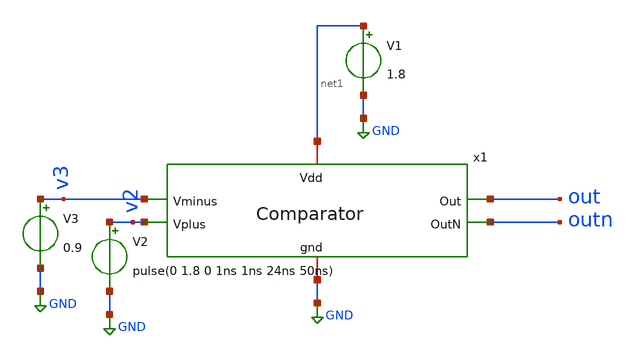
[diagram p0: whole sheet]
** sch_path: xschem/comparator_tb.sch
**.subckt comparator_tb
x1 net1 out outn v3 v2 GND comparator
V1 net1 GND 1.8
V2 v2 GND pulse(0 1.8 0 1ns 1ns 24ns 50ns)
V3 v3 GND 0.9
**** begin user architecture code


.inclue /home/lbraga/Projects/relax_oscillator/mag/comparator.spice
.lib /usr/local/share/pdk/sky130A/libs.tech/ngspice/sky130.lib.spice tt
.control
        tran 0.01n 300ns
  	set color0=rgb:f/f/f
        set xbrushwidth=3
        plot v(v2) v(v3)
	options color3=green
        options color2=orange
	plot v(out) v(outn)
	plot i(v1)
        plot @m.x1.xxm11.x0.msky130_fd_pr__nfet_01v8[id]

.endc
.save all


**** end user architecture code
**.ends

* expanding   symbol:  comparator.sym # of pins=6
** sym_path: xschem/comparator.sym
** sch_path: xschem/comparator.sch
.subckt comparator Vdd Out OutN Vminus Vplus gnd
*.ipin Vminus
*.ipin Vplus
*.iopin Vdd
*.iopin gnd
*.opin OutN
*.opin Out
XM1 net2 net2 Vdd Vdd sky130_fd_pr__pfet_01v8 L=0.75 W=7.5 nf=1 ad='int((nf+1)/2) * W/nf * 0.29' as='int((nf+2)/2) * W/nf * 0.29'
+ pd='2*int((nf+1)/2) * (W/nf + 0.29)' ps='2*int((nf+2)/2) * (W/nf + 0.29)' nrd='0.29 / W' nrs='0.29 / W'
+ sa=0 sb=0 sd=0 mult=1 m=1
XM2 net3 net2 Vdd Vdd sky130_fd_pr__pfet_01v8 L=0.75 W=7.5 nf=1 ad='int((nf+1)/2) * W/nf * 0.29' as='int((nf+2)/2) * W/nf * 0.29'
+ pd='2*int((nf+1)/2) * (W/nf + 0.29)' ps='2*int((nf+2)/2) * (W/nf + 0.29)' nrd='0.29 / W' nrs='0.29 / W'
+ sa=0 sb=0 sd=0 mult=1 m=1
XM5 OutN net3 Vdd Vdd sky130_fd_pr__pfet_01v8 L=0.15 W=1.5 nf=1 ad='int((nf+1)/2) * W/nf * 0.29' as='int((nf+2)/2) * W/nf * 0.29'
+ pd='2*int((nf+1)/2) * (W/nf + 0.29)' ps='2*int((nf+2)/2) * (W/nf + 0.29)' nrd='0.29 / W' nrs='0.29 / W'
+ sa=0 sb=0 sd=0 mult=1 m=1
XM6 OutN net3 gnd gnd sky130_fd_pr__nfet_01v8 L=0.15 W=.75 nf=1 ad='int((nf+1)/2) * W/nf * 0.29' as='int((nf+2)/2) * W/nf * 0.29'
+ pd='2*int((nf+1)/2) * (W/nf + 0.29)' ps='2*int((nf+2)/2) * (W/nf + 0.29)' nrd='0.29 / W' nrs='0.29 / W'
+ sa=0 sb=0 sd=0 mult=1 m=1
XM7 Out OutN Vdd Vdd sky130_fd_pr__pfet_01v8 L=0.15 W=3 nf=1 ad='int((nf+1)/2) * W/nf * 0.29' as='int((nf+2)/2) * W/nf * 0.29'
+ pd='2*int((nf+1)/2) * (W/nf + 0.29)' ps='2*int((nf+2)/2) * (W/nf + 0.29)' nrd='0.29 / W' nrs='0.29 / W'
+ sa=0 sb=0 sd=0 mult=1 m=1
XM8 Out OutN gnd gnd sky130_fd_pr__nfet_01v8 L=0.15 W=1.5 nf=1 ad='int((nf+1)/2) * W/nf * 0.29' as='int((nf+2)/2) * W/nf * 0.29'
+ pd='2*int((nf+1)/2) * (W/nf + 0.29)' ps='2*int((nf+2)/2) * (W/nf + 0.29)' nrd='0.29 / W' nrs='0.29 / W'
+ sa=0 sb=0 sd=0 mult=1 m=1
XM3 net2 Vplus net1 gnd sky130_fd_pr__nfet_01v8 L=0.75 W=3.75 nf=1 ad='int((nf+1)/2) * W/nf * 0.29' as='int((nf+2)/2) * W/nf * 0.29'
+ pd='2*int((nf+1)/2) * (W/nf + 0.29)' ps='2*int((nf+2)/2) * (W/nf + 0.29)' nrd='0.29 / W' nrs='0.29 / W'
+ sa=0 sb=0 sd=0 mult=1 m=1
XM4 net3 Vminus net1 gnd sky130_fd_pr__nfet_01v8 L=0.75 W=3.75 nf=1 ad='int((nf+1)/2) * W/nf * 0.29'
+ as='int((nf+2)/2) * W/nf * 0.29' pd='2*int((nf+1)/2) * (W/nf + 0.29)' ps='2*int((nf+2)/2) * (W/nf + 0.29)'
+ nrd='0.29 / W' nrs='0.29 / W' sa=0 sb=0 sd=0 mult=1 m=1
XM9 net1 net4 gnd gnd sky130_fd_pr__nfet_01v8 L=0.75 W=7 nf=1 ad='int((nf+1)/2) * W/nf * 0.29' as='int((nf+2)/2) * W/nf * 0.29'
+ pd='2*int((nf+1)/2) * (W/nf + 0.29)' ps='2*int((nf+2)/2) * (W/nf + 0.29)' nrd='0.29 / W' nrs='0.29 / W'
+ sa=0 sb=0 sd=0 mult=1 m=1
XM10 net4 net4 gnd gnd sky130_fd_pr__nfet_01v8 L=0.75 W=0.7 nf=1 ad='int((nf+1)/2) * W/nf * 0.29' as='int((nf+2)/2) * W/nf * 0.29'
+ pd='2*int((nf+1)/2) * (W/nf + 0.29)' ps='2*int((nf+2)/2) * (W/nf + 0.29)' nrd='0.29 / W' nrs='0.29 / W'
+ sa=0 sb=0 sd=0 mult=1 m=1
XM11 net5 net4 net6 gnd sky130_fd_pr__nfet_01v8 L=0.75 W=1.4 nf=1 ad='int((nf+1)/2) * W/nf * 0.29' as='int((nf+2)/2) * W/nf * 0.29'
+ pd='2*int((nf+1)/2) * (W/nf + 0.29)' ps='2*int((nf+2)/2) * (W/nf + 0.29)' nrd='0.29 / W' nrs='0.29 / W'
+ sa=0 sb=0 sd=0 mult=1 m=1
XM12 net4 net5 Vdd Vdd sky130_fd_pr__pfet_01v8 L=0.75 W=7.5 nf=1 ad='int((nf+1)/2) * W/nf * 0.29' as='int((nf+2)/2) * W/nf * 0.29'
+ pd='2*int((nf+1)/2) * (W/nf + 0.29)' ps='2*int((nf+2)/2) * (W/nf + 0.29)' nrd='0.29 / W' nrs='0.29 / W'
+ sa=0 sb=0 sd=0 mult=1 m=1
XM13 net5 net5 Vdd Vdd sky130_fd_pr__pfet_01v8 L=0.75 W=7.5 nf=1 ad='int((nf+1)/2) * W/nf * 0.29' as='int((nf+2)/2) * W/nf * 0.29'
+ pd='2*int((nf+1)/2) * (W/nf + 0.29)' ps='2*int((nf+2)/2) * (W/nf + 0.29)' nrd='0.29 / W' nrs='0.29 / W'
+ sa=0 sb=0 sd=0 mult=1 m=1
XR1 gnd net6 gnd sky130_fd_pr__res_xhigh_po_0p35 L=17.45 mult=1 m=1
XR2 Vplus Out gnd sky130_fd_pr__res_xhigh_po W=.35 L=58 mult=1 m=1
.ends

.GLOBAL GND
.end
